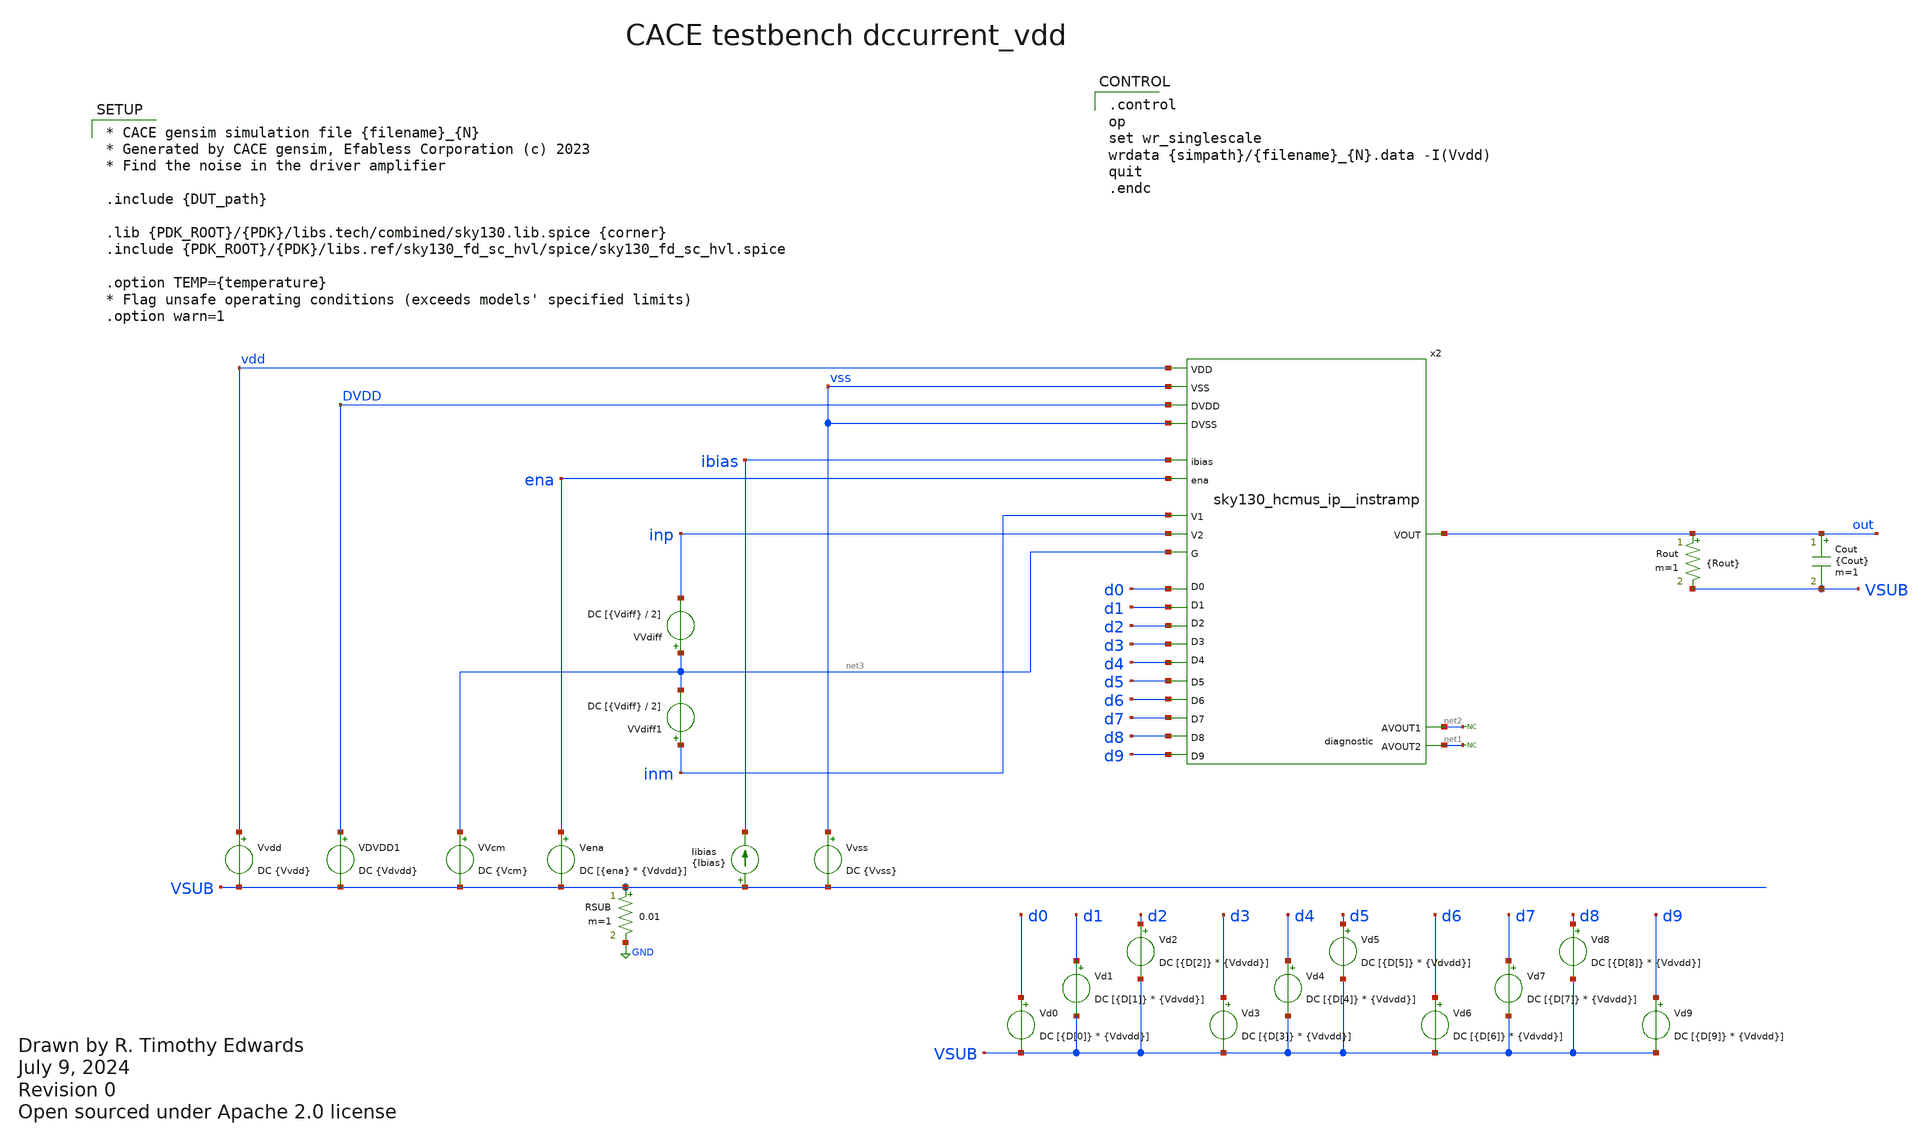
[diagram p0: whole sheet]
** sch_path: cace/templates/dccurrent_vdd.sch
* Open sourced under Apache 2.0 license
**.subckt dccurrent_vdd
VVcm net3 VSUB DC {Vcm}
Vena ena VSUB DC [{ena} * {Vdvdd}]
Vvss vss VSUB DC {Vvss}
Rout out VSUB {Rout} m=1
Cout out VSUB {Cout} m=1
Vvdd vdd VSUB DC {Vvdd}
RSUB VSUB GND 0.01 m=1
VVdiff net3 inp DC [{Vdiff} / 2]
x2 vdd vss net3 inm inp d0 d1 d2 d3 d4 d5 d6 d7 d8 d9 net2 net1 out ibias ena DVDD vss
+ sky130_hcmus_ip__instramp
* noconn #net2
* noconn #net1
VDVDD1 DVDD VSUB DC {Vdvdd}
Iibias VSUB ibias {Ibias}
Vd0 d0 VSUB DC [{D[0]} * {Vdvdd}]
Vd1 d1 VSUB DC [{D[1]} * {Vdvdd}]
Vd2 d2 VSUB DC [{D[2]} * {Vdvdd}]
Vd3 d3 VSUB DC [{D[3]} * {Vdvdd}]
Vd4 d4 VSUB DC [{D[4]} * {Vdvdd}]
Vd5 d5 VSUB DC [{D[5]} * {Vdvdd}]
Vd6 d6 VSUB DC [{D[6]} * {Vdvdd}]
Vd7 d7 VSUB DC [{D[7]} * {Vdvdd}]
Vd8 d8 VSUB DC [{D[8]} * {Vdvdd}]
Vd9 d9 VSUB DC [{D[9]} * {Vdvdd}]
VVdiff1 inm net3 DC [{Vdiff} / 2]
**** begin user architecture code

.control
op
set wr_singlescale
wrdata {simpath}/{filename}_{N}.data -I(Vvdd)
quit
.endc



* CACE gensim simulation file {filename}_{N}
* Generated by CACE gensim, Efabless Corporation (c) 2023
* Find the noise in the driver amplifier

.include {DUT_path}

.lib {PDK_ROOT}/{PDK}/libs.tech/combined/sky130.lib.spice {corner}
.include {PDK_ROOT}/{PDK}/libs.ref/sky130_fd_sc_hvl/spice/sky130_fd_sc_hvl.spice

.option TEMP={temperature}
* Flag unsafe operating conditions (exceeds models' specified limits)
.option warn=1


**** end user architecture code
**.ends
.GLOBAL GND
.end
